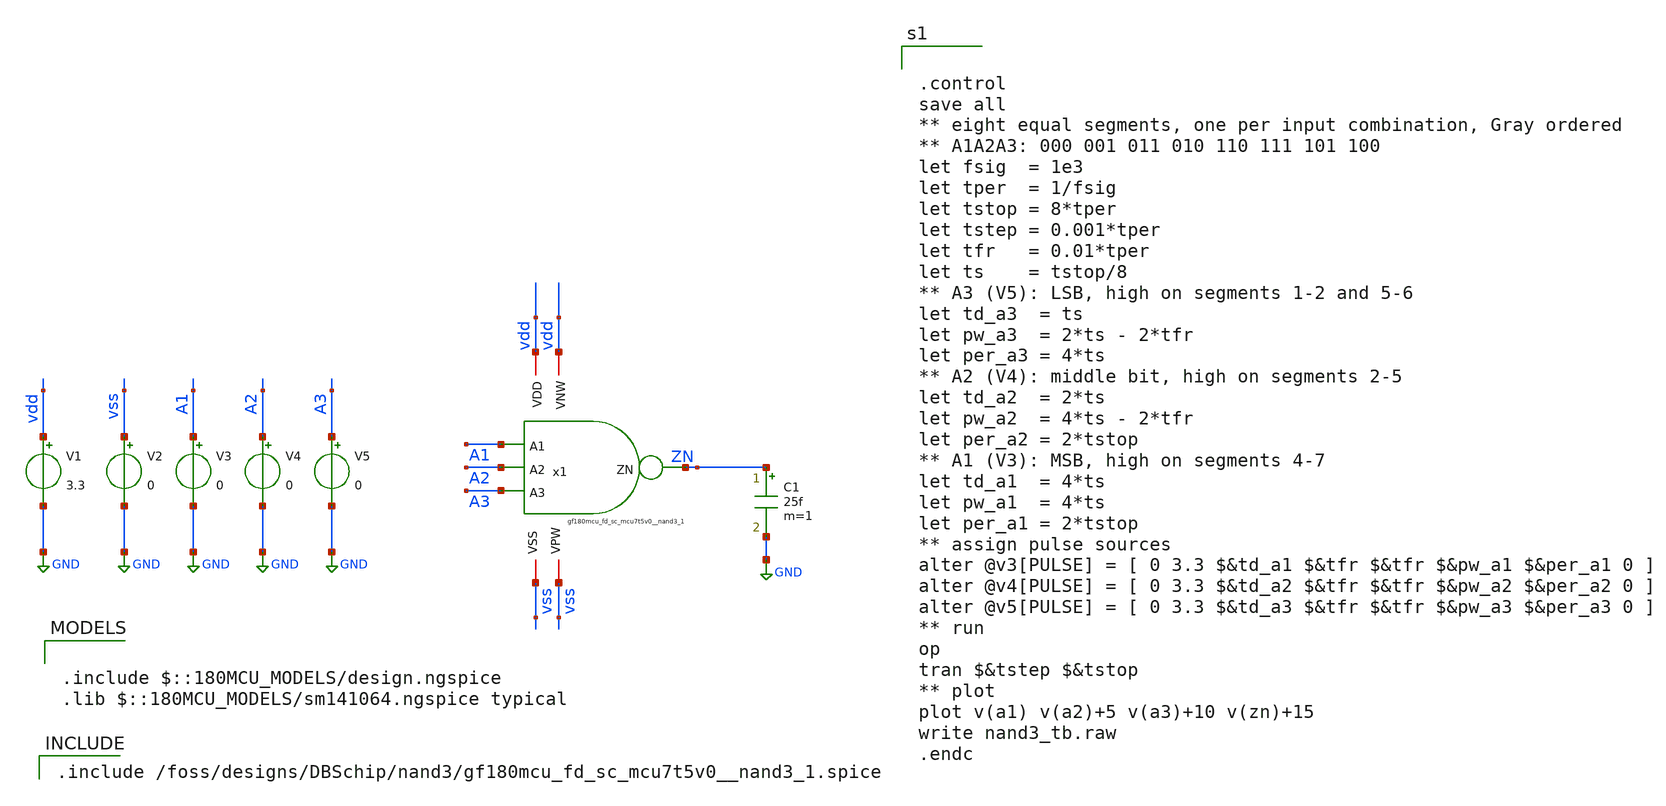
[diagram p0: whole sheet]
** sch_path: nand3/gf180mcu_fd_sc_mcu7t5v0__nand3_1_tb.sch
**.subckt gf180mcu_fd_sc_mcu7t5v0__nand3_1_tb
V1 vdd GND 3.3
V2 vss GND 0
V3 A1 GND 0
V4 A2 GND 0
V5 A3 GND 0
C1 ZN GND 25f m=1
x1 A1 A2 A3 ZN vdd vdd vss vss gf180mcu_fd_sc_mcu7t5v0__nand3_1
**** begin user architecture code

.include $::180MCU_MODELS/design.ngspice
.lib $::180MCU_MODELS/sm141064.ngspice typical


.include /foss/designs/DBSchip/nand3/gf180mcu_fd_sc_mcu7t5v0__nand3_1.spice



.control
save all
** eight equal segments, one per input combination, Gray ordered
** A1A2A3: 000 001 011 010 110 111 101 100
let fsig  = 1e3
let tper  = 1/fsig
let tstop = 8*tper
let tstep = 0.001*tper
let tfr   = 0.01*tper
let ts    = tstop/8
** A3 (V5): LSB, high on segments 1-2 and 5-6
let td_a3  = ts
let pw_a3  = 2*ts - 2*tfr
let per_a3 = 4*ts
** A2 (V4): middle bit, high on segments 2-5
let td_a2  = 2*ts
let pw_a2  = 4*ts - 2*tfr
let per_a2 = 2*tstop
** A1 (V3): MSB, high on segments 4-7
let td_a1  = 4*ts
let pw_a1  = 4*ts
let per_a1 = 2*tstop
** assign pulse sources
alter @v3[PULSE] = [ 0 3.3 $&td_a1 $&tfr $&tfr $&pw_a1 $&per_a1 0 ]
alter @v4[PULSE] = [ 0 3.3 $&td_a2 $&tfr $&tfr $&pw_a2 $&per_a2 0 ]
alter @v5[PULSE] = [ 0 3.3 $&td_a3 $&tfr $&tfr $&pw_a3 $&per_a3 0 ]
** run
op
tran $&tstep $&tstop
** plot
plot v(a1) v(a2)+5 v(a3)+10 v(zn)+15
write nand3_tb.raw
.endc


**** end user architecture code
**.ends
.GLOBAL GND
.end
